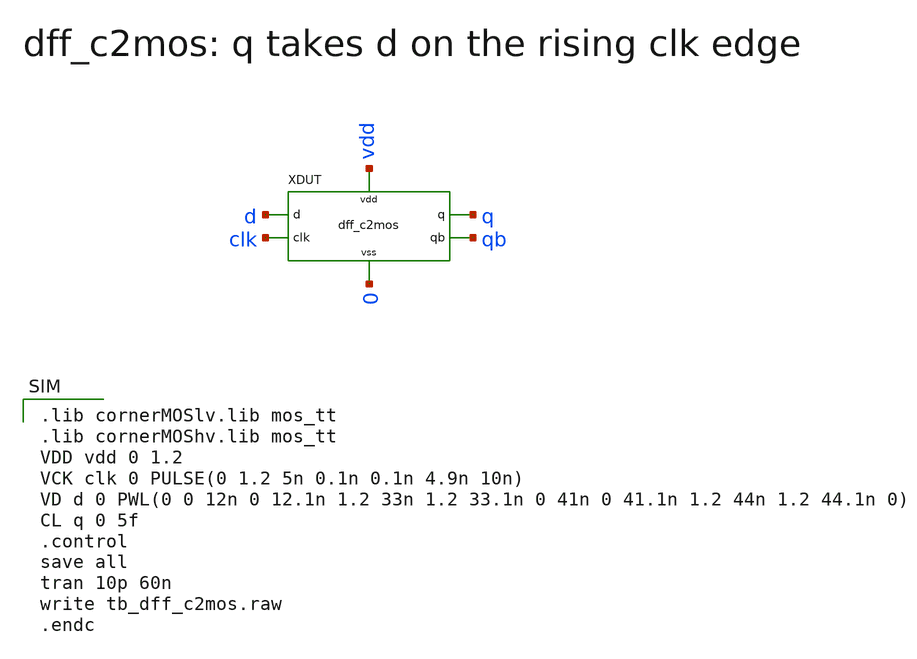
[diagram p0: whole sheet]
** sch_path: verification/tb_dff_c2mos.sch
**.subckt tb_dff_c2mos
XDUT d clk q qb vdd 0 dff_c2mos
**** begin user architecture code

.lib cornerMOSlv.lib mos_tt
.lib cornerMOShv.lib mos_tt
VDD vdd 0 1.2
VCK clk 0 PULSE(0 1.2 5n 0.1n 0.1n 4.9n 10n)
VD d 0 PWL(0 0 12n 0 12.1n 1.2 33n 1.2 33.1n 0 41n 0 41.1n 1.2 44n 1.2 44.1n 0)
CL q 0 5f
.control
save all
tran 10p 60n
write tb_dff_c2mos.raw
.endc

**** end user architecture code
**.ends

* expanding   symbol:  schematics/dff_c2mos.sym # of pins=6
** sym_path: xschem/schematics/dff_c2mos.sym
** sch_path: xschem/schematics/dff_c2mos.sch
.subckt dff_c2mos d clk q qb vdd vss
*.iopin d
*.iopin q
*.iopin qb
*.iopin clk
*.iopin vdd
*.iopin vss
XMT1N net1 clkb d vss sg13_lv_nmos w=0.6u l=0.13u ng=1 m=1
XMT1P d clki net1 vdd sg13_lv_pmos w=1.2u l=0.13u ng=1 m=1
XMT3N net3 clki net2 vss sg13_lv_nmos w=0.6u l=0.13u ng=1 m=1
XMT3P net2 clkb net3 vdd sg13_lv_pmos w=1.2u l=0.13u ng=1 m=1
XMT2P net4 clkb net1 vdd sg13_lv_pmos w=0.6u l=0.13u ng=1 m=1
XMT2N net1 clki net4 vss sg13_lv_nmos w=0.3u l=0.13u ng=1 m=1
XMT4P net5 clki net3 vdd sg13_lv_pmos w=0.6u l=0.13u ng=1 m=1
XMT4N net3 clkb net5 vss sg13_lv_nmos w=0.3u l=0.13u ng=1 m=1
XI1 net2 net1 vdd vss sg13cmos5l_inv_1
XI3 net6 net3 vdd vss sg13cmos5l_inv_1
XI5 qb net6 vdd vss sg13cmos5l_inv_1
XI6 q qb vdd vss sg13cmos5l_inv_1
XI2 net2 net4 vdd vss INVLVW
XI4 net6 net5 vdd vss INVLVW
XI0 clkb clk vdd vss sg13cmos5l_inv_1
XI9 clki clkb vdd vss sg13cmos5l_inv_1
.ends


* expanding   symbol:  logic_gates/sg13cmos5l_inv_1.sym # of pins=4
** sym_path: xschem/logic_gates/sg13cmos5l_inv_1.sym
** sch_path: xschem/logic_gates/sg13cmos5l_inv_1.sch
.subckt sg13cmos5l_inv_1 Y A VDD VSS
*.iopin Y
*.iopin A
*.iopin VDD
*.iopin VSS
XMN0 Y A VSS VSS sg13_lv_nmos w=0.74u l=0.13u ng=1 m=1
XMP0 VDD A Y VDD sg13_lv_pmos w=1.12u l=0.13u ng=1 m=1
.ends


* expanding   symbol:  logic_gates/INVLVW.sym # of pins=4
** sym_path: xschem/logic_gates/INVLVW.sym
** sch_path: xschem/logic_gates/INVLVW.sch
.subckt INVLVW a y vdd vss
*.iopin vdd
*.iopin vss
*.iopin y
*.iopin a
XMP vdd a y vdd sg13_lv_pmos w=0.3u l=0.3u ng=1 m=1
XMN y a vss vss sg13_lv_nmos w=0.3u l=0.3u ng=1 m=1
.ends

.end
